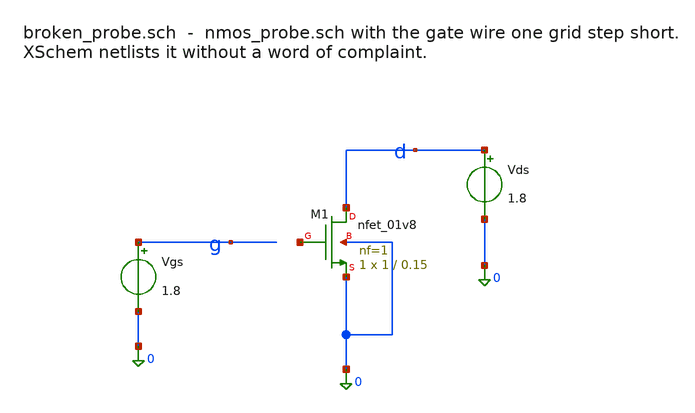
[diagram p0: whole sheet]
** sch_path: labs/lab-01-first-schematic/xschem/broken_probe.sch
**.subckt broken_probe
XM1 d net1 0 0 sky130_fd_pr__nfet_01v8 L=0.15 W=1 nf=1 ad='int((1 + 1)/2) * 1 / 1 * 0.29' as='int((1 + 2)/2) * 1 / 1 * 0.29'
+ pd='2*int((1 + 1)/2) * (1 / 1 + 0.29)' ps='2*int((1 + 2)/2) * (1 / 1 + 0.29)' nrd='0.29 / 1 ' nrs='0.29 / 1 '
+ sa=0 sb=0 sd=0 mult=1 m=1
Vgs g 0 1.8
Vds d 0 1.8
**.ends
.end
